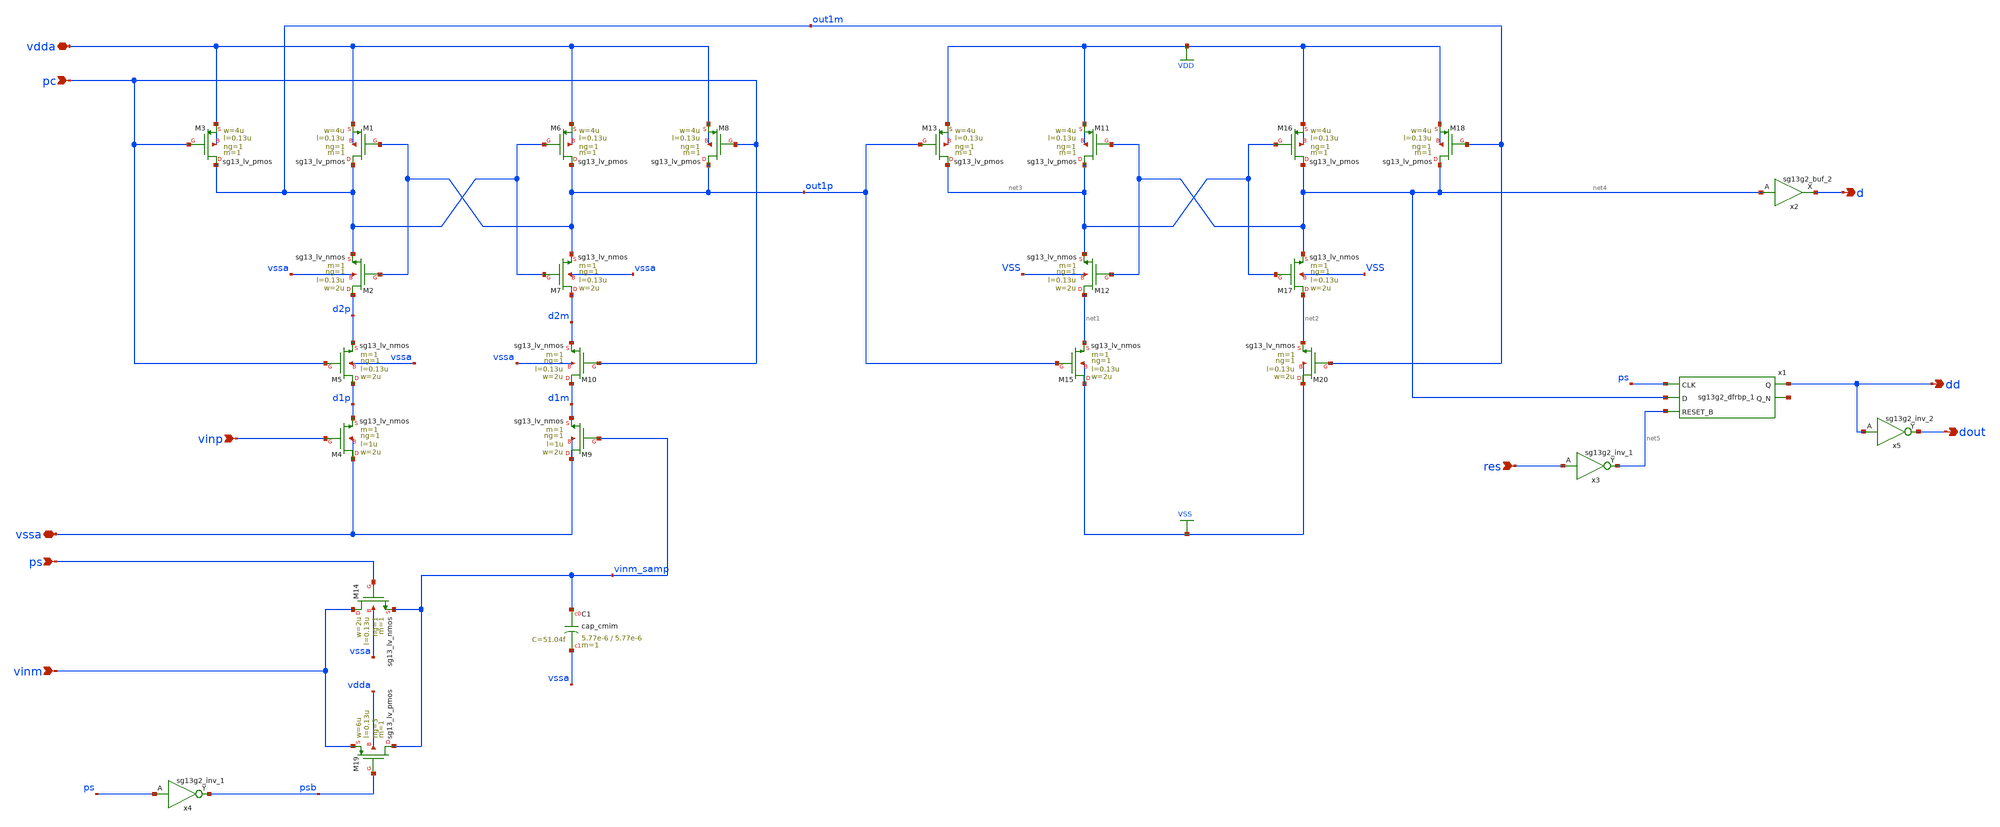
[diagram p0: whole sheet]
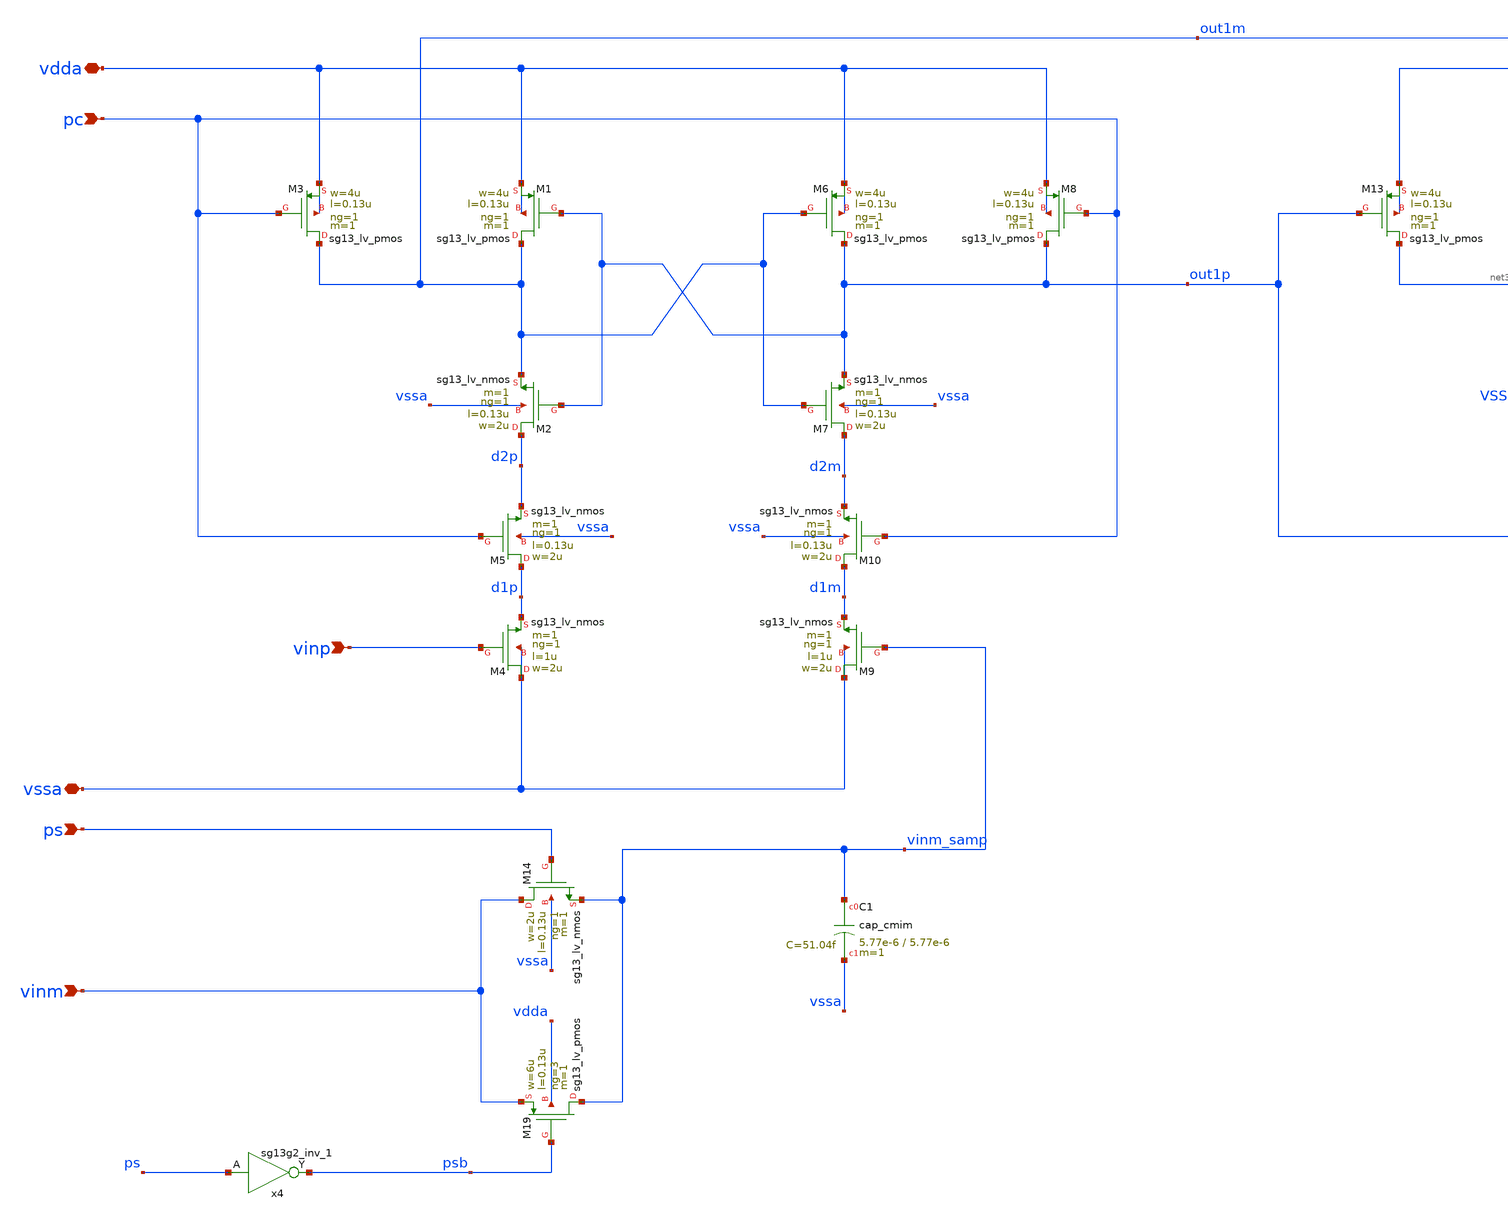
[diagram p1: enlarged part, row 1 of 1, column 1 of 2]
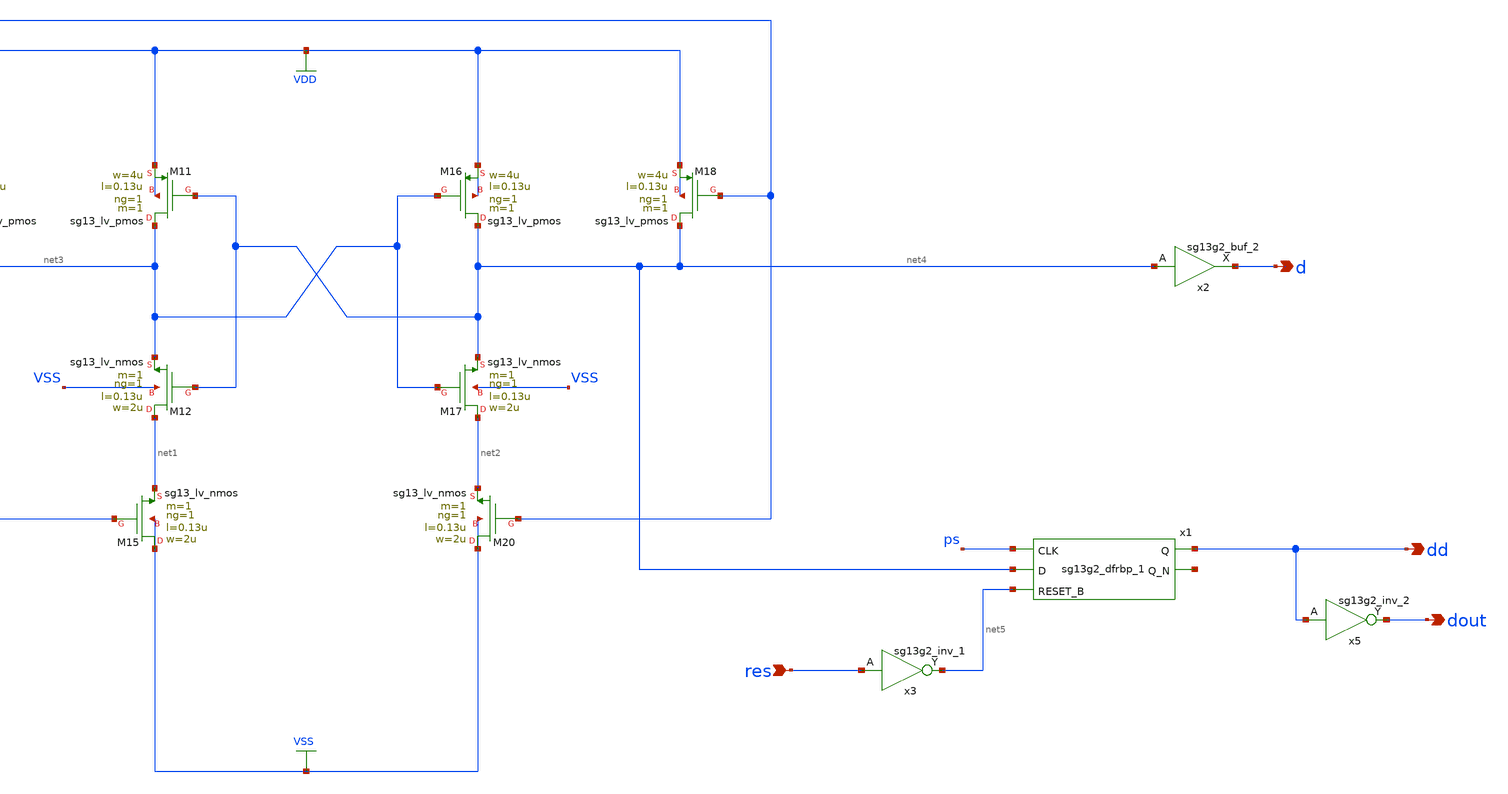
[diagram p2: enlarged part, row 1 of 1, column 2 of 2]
** sch_path: 5_Design/4_Layout/Team 4/xschem/comp_team4.sch
* IHP-GmbH/IHP-Open-PDK/ihp-sg13g2/libs.tech/xschem/sg13g2_stdcells/sg13g2_inv_2.sch:
* Copyright 2023 IHP PDK Authors
* Licensed under the Apache License, Version 2.0 (the "License");
**.subckt comp_team4 vdda vssa pc vinp res ps vinm d dd dout
*.iopin vdda
*.iopin vssa
*.ipin pc
*.ipin vinp
*.ipin res
*.ipin ps
*.ipin vinm
*.opin d
*.opin dd
*.opin dout
XM1 out1m out1p vdda vdda sg13_lv_pmos w=4u l=0.13u ng=1 m=1 mm_ok=1
XM2 d2p out1p out1m vssa sg13_lv_nmos w=2u l=0.13u ng=1 m=1 mm_ok=1
XM3 out1m pc vdda vdda sg13_lv_pmos w=4u l=0.13u ng=1 m=1 mm_ok=1
XM4 vssa vinp d1p vssa sg13_lv_nmos w=2u l=1u ng=1 m=1 mm_ok=1
XM5 d1p pc d2p vssa sg13_lv_nmos w=2u l=0.13u ng=1 m=1 mm_ok=1
XM6 out1p out1m vdda vdda sg13_lv_pmos w=4u l=0.13u ng=1 m=1 mm_ok=1
XM7 d2m out1m out1p vssa sg13_lv_nmos w=2u l=0.13u ng=1 m=1 mm_ok=1
XM8 out1p pc vdda vdda sg13_lv_pmos w=4u l=0.13u ng=1 m=1 mm_ok=1
XM9 vssa vinm_samp d1m vssa sg13_lv_nmos w=2u l=1u ng=1 m=1 mm_ok=1
XM10 d1m pc d2m vssa sg13_lv_nmos w=2u l=0.13u ng=1 m=1 mm_ok=1
XM11 net3 net4 VDD VDD sg13_lv_pmos w=4u l=0.13u ng=1 m=1 mm_ok=1
XM12 net1 net4 net3 VSS sg13_lv_nmos w=2u l=0.13u ng=1 m=1 mm_ok=1
XM13 net3 out1p VDD VDD sg13_lv_pmos w=4u l=0.13u ng=1 m=1 mm_ok=1
XM15 VSS out1p net1 VSS sg13_lv_nmos w=2u l=0.13u ng=1 m=1 mm_ok=1
XM16 net4 net3 VDD VDD sg13_lv_pmos w=4u l=0.13u ng=1 m=1 mm_ok=1
XM17 net2 net3 net4 VSS sg13_lv_nmos w=2u l=0.13u ng=1 m=1 mm_ok=1
XM18 net4 out1m VDD VDD sg13_lv_pmos w=4u l=0.13u ng=1 m=1 mm_ok=1
XM20 VSS out1m net2 VSS sg13_lv_nmos w=2u l=0.13u ng=1 m=1 mm_ok=1
x2 d net4 VDD VSS sg13g2_buf_2
x3 net5 res VDD VSS sg13g2_inv_1
XC1 vinm_samp vssa cap_cmim w=5.77e-6 l=5.77e-6 m=1 mm_ok=1
XM14 vinm ps vinm_samp vssa sg13_lv_nmos w=2u l=0.13u ng=1 m=1 mm_ok=1
XM19 vinm_samp psb vinm vdda sg13_lv_pmos w=6u l=0.13u ng=3 m=1 mm_ok=1
x4 psb ps VDD VSS sg13g2_inv_1
x1 dd net6 ps net4 net5 VDD VSS sg13g2_dfrbp_1
x5 dout dd VDD VSS sg13g2_inv_2
**.ends

* expanding   symbol:  sg13g2_stdcells/sg13g2_buf_2.sym # of pins=2
** sym_path: sg13g2_stdcells/sg13g2_buf_2.sym
** sch_path: sg13g2_stdcells/sg13g2_buf_2.sch
.subckt sg13g2_buf_2 X A VDD VSS
*.ipin A
*.opin X
*.iopin VDD
*.iopin VSS
XM1 net1 A VSS VSS sg13_lv_nmos w=640.00n l=130.00n ng=1 m=1 mm_ok=1
XM2 X net1 VSS VSS sg13_lv_nmos w=1.48u l=130.00n ng=2 m=1 mm_ok=1
XM3 net1 A VDD VDD sg13_lv_pmos w=1.000u l=130.00n ng=1 m=1 mm_ok=1
XM4 X net1 VDD VDD sg13_lv_pmos w=2.24u l=130.00n ng=2 m=1 mm_ok=1
.ends


* expanding   symbol:  sg13g2_stdcells/sg13g2_inv_1.sym # of pins=2
** sym_path: sg13g2_stdcells/sg13g2_inv_1.sym
** sch_path: sg13g2_stdcells/sg13g2_inv_1.sch
.subckt sg13g2_inv_1 Y A VDD VSS
*.opin Y
*.ipin A
*.iopin VDD
*.iopin VSS
XM1 Y A VSS VSS sg13_lv_nmos w=740.00n l=130.00n ng=1 m=1 mm_ok=1
XM2 Y A VDD VDD sg13_lv_pmos w=1.12u l=130.00n ng=1 m=1 mm_ok=1
.ends


* expanding   symbol:  sg13g2_stdcells/sg13g2_dfrbp_1.sym # of pins=5
** sym_path: sg13g2_stdcells/sg13g2_dfrbp_1.sym
** sch_path: sg13g2_stdcells/sg13g2_dfrbp_1.sch
.subckt sg13g2_dfrbp_1 Q Q_N CLK D RESET_B VDD VSS
*.ipin D
*.ipin RESET_B
*.ipin CLK
*.opin Q
*.opin Q_N
*.iopin VDD
*.iopin VSS
XM1 Db D net10 VSS sg13_lv_nmos w=420.00n l=130.00n ng=1 m=1 mm_ok=1
XM2 net10 RESET_B VSS VSS sg13_lv_nmos w=420.00n l=130.00n ng=1 m=1 mm_ok=1
XM3 net1 clkneg net9 VSS sg13_lv_nmos w=420.00n l=130.00n ng=1 m=1 mm_ok=1
XM4 net9 net1 VSS VSS sg13_lv_nmos w=420.00n l=130.00n ng=1 m=1 mm_ok=1
XM5 net1 net1 net5 VSS sg13_lv_nmos w=420.00n l=130.00n ng=1 m=1 mm_ok=1
XM6 net5 RESET_B VSS VSS sg13_lv_nmos w=420.00n l=130.00n ng=1 m=1 mm_ok=1
XM7 Q_N net1 VSS VSS sg13_lv_nmos w=740.00n l=130.00n ng=1 m=1 mm_ok=1
XM8 net2 net1 VSS VSS sg13_lv_nmos w=740.00n l=130.00n ng=1 m=1 mm_ok=1
XM9 Q net2 VSS VSS sg13_lv_nmos w=740.00n l=130.00n ng=1 m=1 mm_ok=1
XM10 clkneg CLK VSS VSS sg13_lv_nmos w=740.00n l=130.00n ng=1 m=1 mm_ok=1
XM11 clkpos clkneg VSS VSS sg13_lv_nmos w=740.00n l=130.00n ng=1 m=1 mm_ok=1
XM12 Db clkneg net3 VSS sg13_lv_nmos w=420.00n l=130.00n ng=1 m=1 mm_ok=1
XM13 net3 clkpos net8 VSS sg13_lv_nmos w=420.00n l=130.00n ng=1 m=1 mm_ok=1
XM14 net8 net3 net4 VSS sg13_lv_nmos w=420.00n l=130.00n ng=1 m=1 mm_ok=1
XM15 net4 RESET_B VSS VSS sg13_lv_nmos w=420.00n l=130.00n ng=1 m=1 mm_ok=1
XM16 net3 net3 VSS VSS sg13_lv_nmos w=740.00n l=130.00n ng=1 m=1 mm_ok=1
XM17 net3 clkpos net1 VSS sg13_lv_nmos w=740.00n l=130.00n ng=1 m=1 mm_ok=1
XM18 Db RESET_B VDD VDD sg13_lv_pmos w=420.00n l=130.00n ng=1 m=1 mm_ok=1
XM19 Db D VDD VDD sg13_lv_pmos w=420.00n l=130.00n ng=1 m=1 mm_ok=1
XM20 net7 net1 VDD VDD sg13_lv_pmos w=420.00n l=130.00n ng=1 m=1 mm_ok=1
XM21 net1 clkpos net7 VDD sg13_lv_pmos w=420.00n l=130.00n ng=1 m=1 mm_ok=1
XM22 net1 net1 VDD VDD sg13_lv_pmos w=420.00n l=130.00n ng=1 m=1 mm_ok=1
XM23 net1 RESET_B VDD VDD sg13_lv_pmos w=420.00n l=130.00n ng=1 m=1 mm_ok=1
XM24 Q_N net1 VDD VDD sg13_lv_pmos w=1.12u l=130.00n ng=1 m=1 mm_ok=1
XM25 net2 net1 VDD VDD sg13_lv_pmos w=1.12u l=130.00n ng=1 m=1 mm_ok=1
XM26 Q net2 VDD VDD sg13_lv_pmos w=1.12u l=130.00n ng=1 m=1 mm_ok=1
XM27 clkneg CLK VDD VDD sg13_lv_pmos w=1.12u l=130.00n ng=1 m=1 mm_ok=1
XM28 clkpos clkneg VDD VDD sg13_lv_pmos w=1.12u l=130.00n ng=1 m=1 mm_ok=1
XM29 Db clkpos net3 VDD sg13_lv_pmos w=420.00n l=130.00n ng=1 m=1 mm_ok=1
XM30 net6 net3 VDD VDD sg13_lv_pmos w=420.00n l=130.00n ng=1 m=1 mm_ok=1
XM31 net3 clkneg net6 VDD sg13_lv_pmos w=420.00n l=130.00n ng=1 m=1 mm_ok=1
XM32 net3 RESET_B VDD VDD sg13_lv_pmos w=420.00n l=130.00n ng=1 m=1 mm_ok=1
XM33 net3 net3 VDD VDD sg13_lv_pmos w=1.000u l=130.00n ng=1 m=1 mm_ok=1
XM34 net3 clkneg net1 VDD sg13_lv_pmos w=1.000u l=130.00n ng=1 m=1 mm_ok=1
.ends


* expanding   symbol:  sg13g2_stdcells/sg13g2_inv_2.sym # of pins=2
** sym_path: sg13g2_stdcells/sg13g2_inv_2.sym
** sch_path: sg13g2_stdcells/sg13g2_inv_2.sch
.subckt sg13g2_inv_2 Y A VDD VSS
*.opin Y
*.ipin A
*.iopin VDD
*.iopin VSS
XM1 Y A VSS VSS sg13_lv_nmos w=1.48u l=130.00n ng=2 m=1 mm_ok=1
XM2 Y A VDD VDD sg13_lv_pmos w=2.24u l=130.00n ng=2 m=1 mm_ok=1
.ends

.GLOBAL VDD
.GLOBAL VSS
.end
